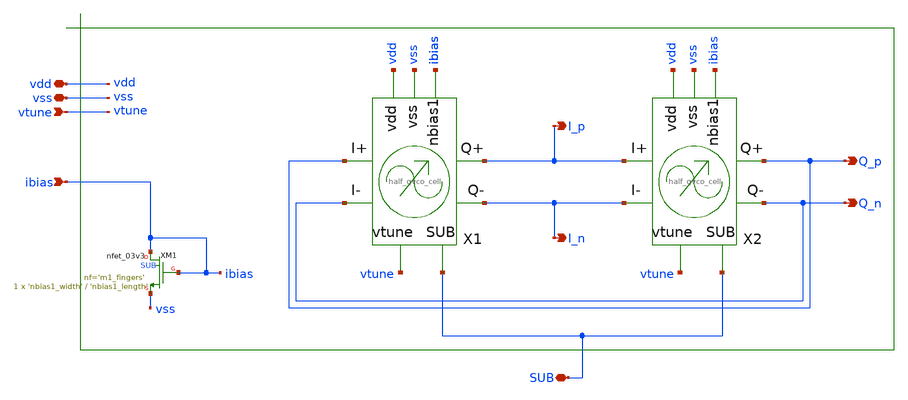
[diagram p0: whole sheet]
** sch_path: sch/vco/vco_quadrature_lc.sch
**.subckt vco_quadrature_lc vdd vss vtune I_p I_n Q_p Q_n ibias SUB
*.iopin vdd
*.iopin vss
*.ipin vtune
*.opin I_p
*.opin I_n
*.opin Q_p
*.opin Q_n
*.ipin ibias
*.iopin SUB
X1 vdd vss ibias Q_p Q_n I_p I_n vtune SUB half_qvco_cell m1m2_width='m1m2_width' m1m2_length='m1m2_length'
+ m1m2_fingers='m1m2_fingers' m1m2_mult='m1m2_mult' m3m4_width='m3m4_width' m3m4_length='m3m4_length' m3m4_fingers='m3m4_fingers'
+ m3m4_mult='m3m4_mult' m5_width='m5_width_matched' m5_length='m5_length_matched' m5_fingers='m5_fingers'
+ m5_mult='m5_mult' capvar_width='capvar_width_total' capvar_length='capvar_length'
X2 vdd vss ibias I_p I_n Q_p Q_n vtune SUB half_qvco_cell m1m2_width='m1m2_width' m1m2_length='m1m2_length'
+ m1m2_fingers='m1m2_fingers' m1m2_mult='m1m2_mult' m3m4_width='m3m4_width' m3m4_length='m3m4_length' m3m4_fingers='m3m4_fingers'
+ m3m4_mult='m3m4_mult' m5_width='m5_width_matched' m5_length='m5_length_matched' m5_fingers='m5_fingers'
+ m5_mult='m5_mult' capvar_width='capvar_width_total' capvar_length='capvar_length'
XM1 ibias ibias vss SUB nfet_03v3 L='nbias1_length' W='nbias1_width' nf='m1_fingers' ad='int((nf+1)/2) * W/nf * 0.18u'
+ as='int((nf+2)/2) * W/nf * 0.18u' pd='2*int((nf+1)/2) * (W/nf + 0.18u)' ps='2*int((nf+2)/2) * (W/nf + 0.18u)'
+ nrd='0.18u / W' nrs='0.18u / W' sa=0 sb=0 sd=0 m=1 par=1
**.ends
.end
